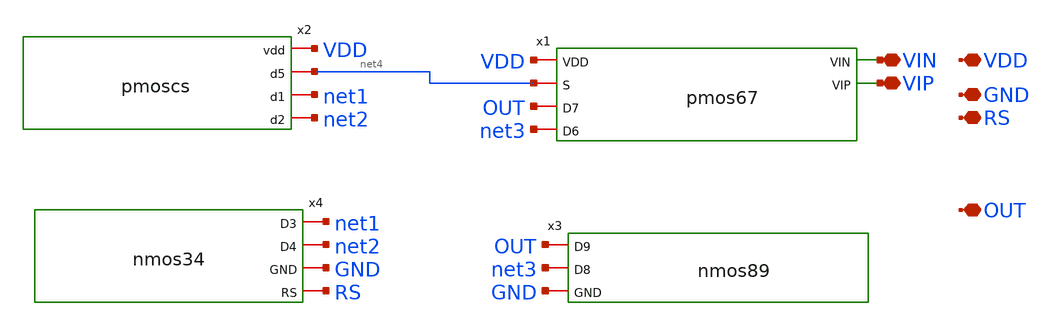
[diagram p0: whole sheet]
** sch_path: opamp/mag/opamp.sch
**.subckt opamp VDD GND RS VIN VIP OUT
*.iopin VDD
*.iopin GND
*.iopin RS
*.iopin VIN
*.iopin VIP
*.iopin OUT
x1 VDD net4 VIN VIP OUT net3 pmos67
x2 VDD net4 net1 net2 pmoscs
x3 OUT net3 GND nmos89
x4 net1 net2 GND RS nmos34
**.ends
.end
